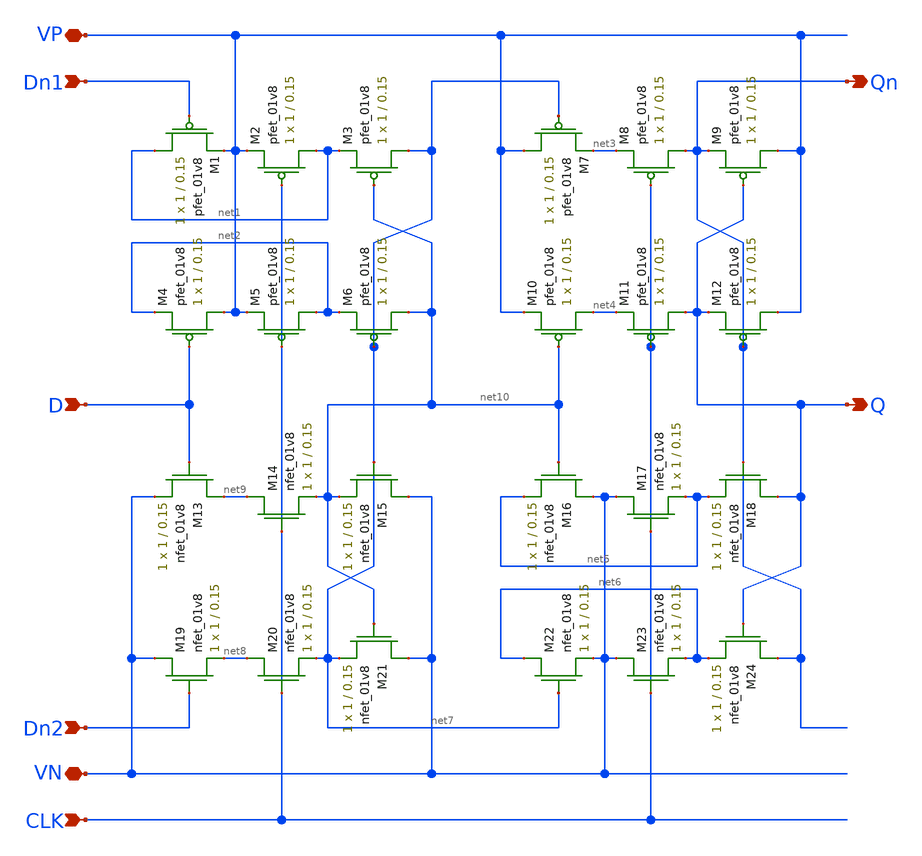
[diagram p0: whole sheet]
** sch_path: MP2/xschem/dff.sch
**.subckt dff Qn Q Dn1 D Dn2 CLK VP VN
*.opin Qn
*.opin Q
*.ipin Dn1
*.ipin D
*.ipin Dn2
*.ipin CLK
*.iopin VP
*.iopin VN
XM1 net1 Dn1 VP VDD sky130_fd_pr__pfet_01v8 L=0.15 W=1 nf=1 ad='int((nf+1)/2) * W/nf * 0.29' as='int((nf+2)/2) * W/nf * 0.29'
+ pd='2*int((nf+1)/2) * (W/nf + 0.29)' ps='2*int((nf+2)/2) * (W/nf + 0.29)' nrd='0.29 / W' nrs='0.29 / W'
+ sa=0 sb=0 sd=0 mult=1 m=1
XM2 net1 CLK VP VDD sky130_fd_pr__pfet_01v8 L=0.15 W=1 nf=1 ad='int((nf+1)/2) * W/nf * 0.29' as='int((nf+2)/2) * W/nf * 0.29'
+ pd='2*int((nf+1)/2) * (W/nf + 0.29)' ps='2*int((nf+2)/2) * (W/nf + 0.29)' nrd='0.29 / W' nrs='0.29 / W'
+ sa=0 sb=0 sd=0 mult=1 m=1
XM3 net7 net10 net1 VDD sky130_fd_pr__pfet_01v8 L=0.15 W=1 nf=1 ad='int((nf+1)/2) * W/nf * 0.29' as='int((nf+2)/2) * W/nf * 0.29'
+ pd='2*int((nf+1)/2) * (W/nf + 0.29)' ps='2*int((nf+2)/2) * (W/nf + 0.29)' nrd='0.29 / W' nrs='0.29 / W'
+ sa=0 sb=0 sd=0 mult=1 m=1
XM4 VP D net2 VDD sky130_fd_pr__pfet_01v8 L=0.15 W=1 nf=1 ad='int((nf+1)/2) * W/nf * 0.29' as='int((nf+2)/2) * W/nf * 0.29'
+ pd='2*int((nf+1)/2) * (W/nf + 0.29)' ps='2*int((nf+2)/2) * (W/nf + 0.29)' nrd='0.29 / W' nrs='0.29 / W'
+ sa=0 sb=0 sd=0 mult=1 m=1
XM5 net2 CLK VP VDD sky130_fd_pr__pfet_01v8 L=0.15 W=1 nf=1 ad='int((nf+1)/2) * W/nf * 0.29' as='int((nf+2)/2) * W/nf * 0.29'
+ pd='2*int((nf+1)/2) * (W/nf + 0.29)' ps='2*int((nf+2)/2) * (W/nf + 0.29)' nrd='0.29 / W' nrs='0.29 / W'
+ sa=0 sb=0 sd=0 mult=1 m=1
XM6 net10 net7 net2 VDD sky130_fd_pr__pfet_01v8 L=0.15 W=1 nf=1 ad='int((nf+1)/2) * W/nf * 0.29' as='int((nf+2)/2) * W/nf * 0.29'
+ pd='2*int((nf+1)/2) * (W/nf + 0.29)' ps='2*int((nf+2)/2) * (W/nf + 0.29)' nrd='0.29 / W' nrs='0.29 / W'
+ sa=0 sb=0 sd=0 mult=1 m=1
XM7 VP net7 net3 VDD sky130_fd_pr__pfet_01v8 L=0.15 W=1 nf=1 ad='int((nf+1)/2) * W/nf * 0.29' as='int((nf+2)/2) * W/nf * 0.29'
+ pd='2*int((nf+1)/2) * (W/nf + 0.29)' ps='2*int((nf+2)/2) * (W/nf + 0.29)' nrd='0.29 / W' nrs='0.29 / W'
+ sa=0 sb=0 sd=0 mult=1 m=1
XM8 Qn CLK net3 VDD sky130_fd_pr__pfet_01v8 L=0.15 W=1 nf=1 ad='int((nf+1)/2) * W/nf * 0.29' as='int((nf+2)/2) * W/nf * 0.29'
+ pd='2*int((nf+1)/2) * (W/nf + 0.29)' ps='2*int((nf+2)/2) * (W/nf + 0.29)' nrd='0.29 / W' nrs='0.29 / W'
+ sa=0 sb=0 sd=0 mult=1 m=1
XM9 VP Q Qn VDD sky130_fd_pr__pfet_01v8 L=0.15 W=1 nf=1 ad='int((nf+1)/2) * W/nf * 0.29' as='int((nf+2)/2) * W/nf * 0.29'
+ pd='2*int((nf+1)/2) * (W/nf + 0.29)' ps='2*int((nf+2)/2) * (W/nf + 0.29)' nrd='0.29 / W' nrs='0.29 / W'
+ sa=0 sb=0 sd=0 mult=1 m=1
XM10 net4 net10 VP VDD sky130_fd_pr__pfet_01v8 L=0.15 W=1 nf=1 ad='int((nf+1)/2) * W/nf * 0.29' as='int((nf+2)/2) * W/nf * 0.29'
+ pd='2*int((nf+1)/2) * (W/nf + 0.29)' ps='2*int((nf+2)/2) * (W/nf + 0.29)' nrd='0.29 / W' nrs='0.29 / W'
+ sa=0 sb=0 sd=0 mult=1 m=1
XM11 Q CLK net4 VDD sky130_fd_pr__pfet_01v8 L=0.15 W=1 nf=1 ad='int((nf+1)/2) * W/nf * 0.29' as='int((nf+2)/2) * W/nf * 0.29'
+ pd='2*int((nf+1)/2) * (W/nf + 0.29)' ps='2*int((nf+2)/2) * (W/nf + 0.29)' nrd='0.29 / W' nrs='0.29 / W'
+ sa=0 sb=0 sd=0 mult=1 m=1
XM12 VP Qn Q VDD sky130_fd_pr__pfet_01v8 L=0.15 W=1 nf=1 ad='int((nf+1)/2) * W/nf * 0.29' as='int((nf+2)/2) * W/nf * 0.29'
+ pd='2*int((nf+1)/2) * (W/nf + 0.29)' ps='2*int((nf+2)/2) * (W/nf + 0.29)' nrd='0.29 / W' nrs='0.29 / W'
+ sa=0 sb=0 sd=0 mult=1 m=1
XM13 net9 D VN GND sky130_fd_pr__nfet_01v8 L=0.15 W=1 nf=1 ad='int((nf+1)/2) * W/nf * 0.29' as='int((nf+2)/2) * W/nf * 0.29'
+ pd='2*int((nf+1)/2) * (W/nf + 0.29)' ps='2*int((nf+2)/2) * (W/nf + 0.29)' nrd='0.29 / W' nrs='0.29 / W'
+ sa=0 sb=0 sd=0 mult=1 m=1
XM14 net9 CLK net10 GND sky130_fd_pr__nfet_01v8 L=0.15 W=1 nf=1 ad='int((nf+1)/2) * W/nf * 0.29' as='int((nf+2)/2) * W/nf * 0.29'
+ pd='2*int((nf+1)/2) * (W/nf + 0.29)' ps='2*int((nf+2)/2) * (W/nf + 0.29)' nrd='0.29 / W' nrs='0.29 / W'
+ sa=0 sb=0 sd=0 mult=1 m=1
XM15 VN net7 net10 GND sky130_fd_pr__nfet_01v8 L=0.15 W=1 nf=1 ad='int((nf+1)/2) * W/nf * 0.29' as='int((nf+2)/2) * W/nf * 0.29'
+ pd='2*int((nf+1)/2) * (W/nf + 0.29)' ps='2*int((nf+2)/2) * (W/nf + 0.29)' nrd='0.29 / W' nrs='0.29 / W'
+ sa=0 sb=0 sd=0 mult=1 m=1
XM16 VN net10 net5 GND sky130_fd_pr__nfet_01v8 L=0.15 W=1 nf=1 ad='int((nf+1)/2) * W/nf * 0.29' as='int((nf+2)/2) * W/nf * 0.29'
+ pd='2*int((nf+1)/2) * (W/nf + 0.29)' ps='2*int((nf+2)/2) * (W/nf + 0.29)' nrd='0.29 / W' nrs='0.29 / W'
+ sa=0 sb=0 sd=0 mult=1 m=1
XM17 VN CLK net5 GND sky130_fd_pr__nfet_01v8 L=0.15 W=1 nf=1 ad='int((nf+1)/2) * W/nf * 0.29' as='int((nf+2)/2) * W/nf * 0.29'
+ pd='2*int((nf+1)/2) * (W/nf + 0.29)' ps='2*int((nf+2)/2) * (W/nf + 0.29)' nrd='0.29 / W' nrs='0.29 / W'
+ sa=0 sb=0 sd=0 mult=1 m=1
XM18 Q Qn net5 GND sky130_fd_pr__nfet_01v8 L=0.15 W=1 nf=1 ad='int((nf+1)/2) * W/nf * 0.29' as='int((nf+2)/2) * W/nf * 0.29'
+ pd='2*int((nf+1)/2) * (W/nf + 0.29)' ps='2*int((nf+2)/2) * (W/nf + 0.29)' nrd='0.29 / W' nrs='0.29 / W'
+ sa=0 sb=0 sd=0 mult=1 m=1
XM19 VN Dn2 net8 GND sky130_fd_pr__nfet_01v8 L=0.15 W=1 nf=1 ad='int((nf+1)/2) * W/nf * 0.29' as='int((nf+2)/2) * W/nf * 0.29'
+ pd='2*int((nf+1)/2) * (W/nf + 0.29)' ps='2*int((nf+2)/2) * (W/nf + 0.29)' nrd='0.29 / W' nrs='0.29 / W'
+ sa=0 sb=0 sd=0 mult=1 m=1
XM20 net8 CLK net7 GND sky130_fd_pr__nfet_01v8 L=0.15 W=1 nf=1 ad='int((nf+1)/2) * W/nf * 0.29' as='int((nf+2)/2) * W/nf * 0.29'
+ pd='2*int((nf+1)/2) * (W/nf + 0.29)' ps='2*int((nf+2)/2) * (W/nf + 0.29)' nrd='0.29 / W' nrs='0.29 / W'
+ sa=0 sb=0 sd=0 mult=1 m=1
XM21 VN net10 net7 GND sky130_fd_pr__nfet_01v8 L=0.15 W=1 nf=1 ad='int((nf+1)/2) * W/nf * 0.29' as='int((nf+2)/2) * W/nf * 0.29'
+ pd='2*int((nf+1)/2) * (W/nf + 0.29)' ps='2*int((nf+2)/2) * (W/nf + 0.29)' nrd='0.29 / W' nrs='0.29 / W'
+ sa=0 sb=0 sd=0 mult=1 m=1
XM22 net6 net7 VN GND sky130_fd_pr__nfet_01v8 L=0.15 W=1 nf=1 ad='int((nf+1)/2) * W/nf * 0.29' as='int((nf+2)/2) * W/nf * 0.29'
+ pd='2*int((nf+1)/2) * (W/nf + 0.29)' ps='2*int((nf+2)/2) * (W/nf + 0.29)' nrd='0.29 / W' nrs='0.29 / W'
+ sa=0 sb=0 sd=0 mult=1 m=1
XM23 VN CLK net6 GND sky130_fd_pr__nfet_01v8 L=0.15 W=1 nf=1 ad='int((nf+1)/2) * W/nf * 0.29' as='int((nf+2)/2) * W/nf * 0.29'
+ pd='2*int((nf+1)/2) * (W/nf + 0.29)' ps='2*int((nf+2)/2) * (W/nf + 0.29)' nrd='0.29 / W' nrs='0.29 / W'
+ sa=0 sb=0 sd=0 mult=1 m=1
XM24 Qn Q net6 GND sky130_fd_pr__nfet_01v8 L=0.15 W=1 nf=1 ad='int((nf+1)/2) * W/nf * 0.29' as='int((nf+2)/2) * W/nf * 0.29'
+ pd='2*int((nf+1)/2) * (W/nf + 0.29)' ps='2*int((nf+2)/2) * (W/nf + 0.29)' nrd='0.29 / W' nrs='0.29 / W'
+ sa=0 sb=0 sd=0 mult=1 m=1
**.ends
.end
